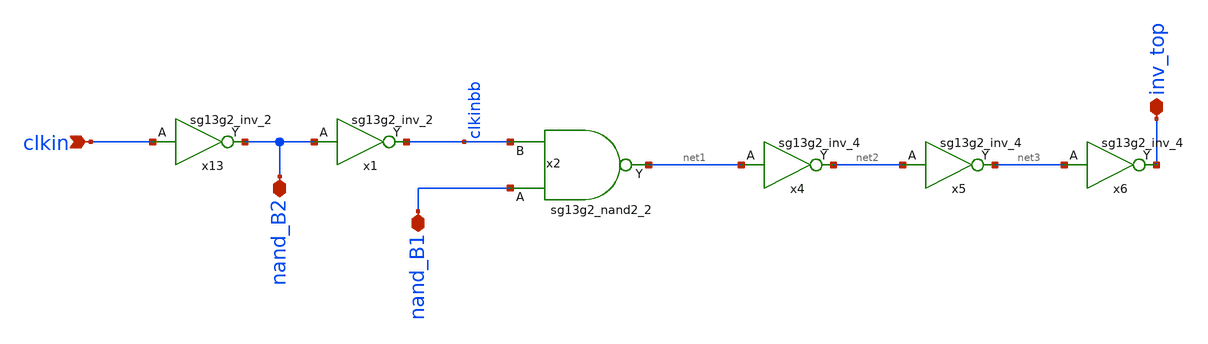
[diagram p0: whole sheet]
** sch_path: 5_Design/4_Layout/Team 5/splitUpSimulationsAndSchematics/clock_5_split3.sch
* IHP-GmbH/IHP-Open-PDK/ihp-sg13g2/libs.tech/xschem/sg13g2_stdcells/sg13g2_inv_2.sch:
* Copyright 2023 IHP PDK Authors
* Licensed under the Apache License, Version 2.0 (the "License");
**.subckt clock_5_split3 clkin nand_B2 nand_B1 inv_top
*.ipin clkin
*.iopin nand_B2
*.iopin nand_B1
*.iopin inv_top
x4 net2 net1 VDD VSS sg13g2_inv_4
x5 net3 net2 VDD VSS sg13g2_inv_4
x6 inv_top net3 VDD VSS sg13g2_inv_4
x13 nand_B2 clkin VDD VSS sg13g2_inv_2
x1 clkinbb nand_B2 VDD VSS sg13g2_inv_2
x2 net1 nand_B1 clkinbb VDD VSS sg13g2_nand2_2
**.ends

* expanding   symbol:  sg13g2_stdcells/sg13g2_inv_4.sym # of pins=2
** sym_path: sg13g2_stdcells/sg13g2_inv_4.sym
** sch_path: sg13g2_stdcells/sg13g2_inv_4.sch
.subckt sg13g2_inv_4 Y A VDD VSS
*.ipin A
*.opin Y
*.iopin VDD
*.iopin VSS
XM1 Y A VSS VSS sg13_lv_nmos w=2.96u l=130.00n ng=4 m=1 mm_ok=1
XM2 Y A VDD VDD sg13_lv_pmos w=4.48u l=130.00n ng=4 m=1 mm_ok=1
.ends


* expanding   symbol:  sg13g2_stdcells/sg13g2_inv_2.sym # of pins=2
** sym_path: sg13g2_stdcells/sg13g2_inv_2.sym
** sch_path: sg13g2_stdcells/sg13g2_inv_2.sch
.subckt sg13g2_inv_2 Y A VDD VSS
*.opin Y
*.ipin A
*.iopin VDD
*.iopin VSS
XM1 Y A VSS VSS sg13_lv_nmos w=1.48u l=130.00n ng=2 m=1 mm_ok=1
XM2 Y A VDD VDD sg13_lv_pmos w=2.24u l=130.00n ng=2 m=1 mm_ok=1
.ends


* expanding   symbol:  sg13g2_stdcells/sg13g2_nand2_2.sym # of pins=3
** sym_path: sg13g2_stdcells/sg13g2_nand2_2.sym
** sch_path: sg13g2_stdcells/sg13g2_nand2_2.sch
.subckt sg13g2_nand2_2 Y A B VDD VSS
*.iopin VDD
*.iopin VSS
*.opin Y
*.ipin B
*.ipin A
XM1 Y A net1 VSS sg13_lv_nmos w=1.44u l=130.00n ng=2 m=1 mm_ok=1
XM2 net1 B VSS VSS sg13_lv_nmos w=1.44u l=130.00n ng=2 m=1 mm_ok=1
XM3 Y A VDD VDD sg13_lv_pmos w=2.24u l=130.00n ng=2 m=1 mm_ok=1
XM4 Y B VDD VDD sg13_lv_pmos w=2.24u l=130.00n ng=2 m=1 mm_ok=1
.ends

.end
